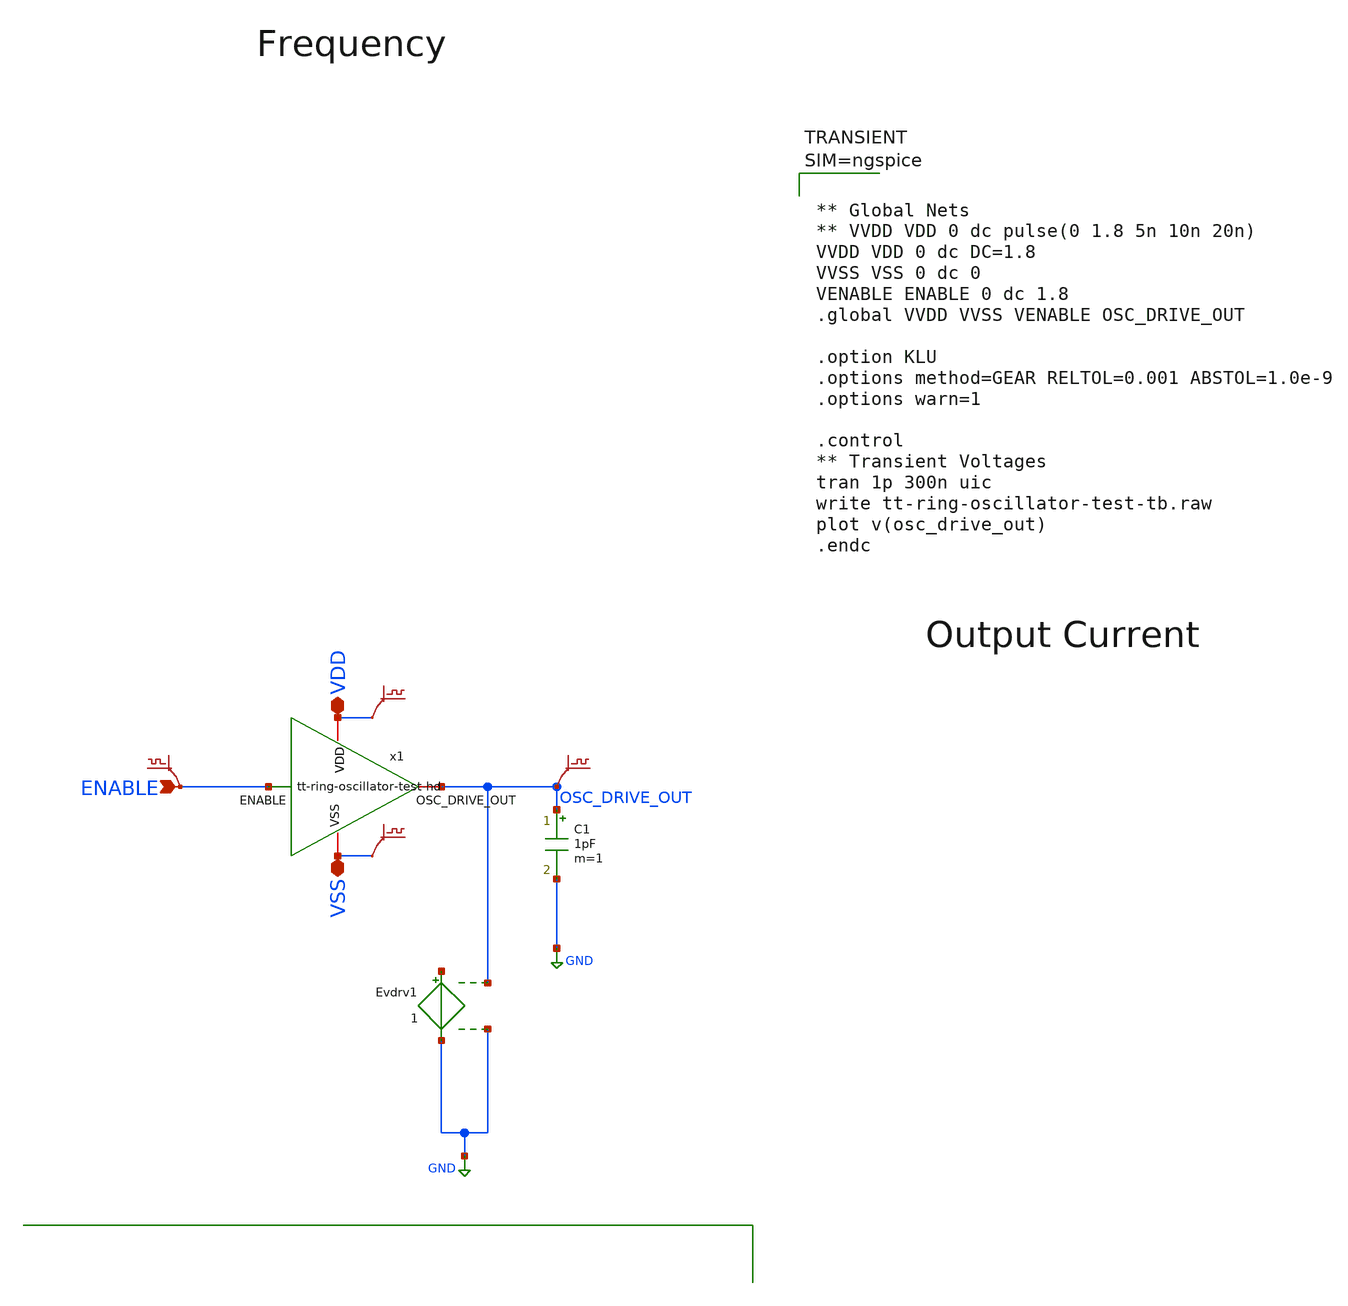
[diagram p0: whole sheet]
** sch_path: xschem/tt-ring-oscillator-test-tb.sch
**.subckt tt-ring-oscillator-test-tb ENABLE VDD VSS
*.ipin ENABLE
*.iopin VDD
*.iopin VSS
C1 OSC_DRIVE_OUT GND 1pF m=1
Evdrv1 net1 GND OSC_DRIVE_OUT GND 1
.save v(osc_drive_out)
.save v(enable)
.save i(vvdd)
.save v(vdd)
.save i(vvss)
.save v(vss)
x1 VDD VSS OSC_DRIVE_OUT ENABLE tt-ring-oscillator-test-hd
**** begin user architecture code

.lib     $::SKYWATER_MODELS/sky130.lib.spice tt
.include $::SKYWATER_STDCELLS/sky130_fd_sc_hd.spice




** Global Nets
** VVDD VDD 0 dc pulse(0 1.8 5n 10n 20n)
VVDD VDD 0 dc DC=1.8
VVSS VSS 0 dc 0
VENABLE ENABLE 0 dc 1.8
.global VVDD VVSS VENABLE OSC_DRIVE_OUT

.option KLU
.options method=GEAR RELTOL=0.001 ABSTOL=1.0e-9
.options warn=1

.control
** Transient Voltages
tran 1p 300n uic
write tt-ring-oscillator-test-tb.raw
plot v(osc_drive_out)
.endc



**** end user architecture code
**.ends

* expanding   symbol:  tt-ring-oscillator-test-hd.sym # of pins=4
** sym_path: xschem/tt-ring-oscillator-test-hd.sym
** sch_path: xschem/tt-ring-oscillator-test-hd.sch
.subckt tt-ring-oscillator-test-hd VDD VSS OSC_DRIVE_OUT ENABLE
*.ipin ENABLE
*.iopin VDD
*.iopin VSS
*.opin OSC_DRIVE_OUT
x1 net29 VSS VSS VDD VDD net1 sky130_fd_sc_hd__inv_1
x2 net1 VSS VSS VDD VDD net9 sky130_fd_sc_hd__inv_1
x3 net9 VSS VSS VDD VDD net2 sky130_fd_sc_hd__inv_1
x4 net2 VSS VSS VDD VDD net22 sky130_fd_sc_hd__inv_1
x5 net22 VSS VSS VDD VDD net21 sky130_fd_sc_hd__inv_1
x6 net21 VSS VSS VDD VDD net20 sky130_fd_sc_hd__inv_1
x7 net20 VSS VSS VDD VDD net27 sky130_fd_sc_hd__inv_1
x9 net27 VSS VSS VDD VDD net10 sky130_fd_sc_hd__inv_1
x10 net10 VSS VSS VDD VDD net3 sky130_fd_sc_hd__inv_1
x11 net3 VSS VSS VDD VDD net23 sky130_fd_sc_hd__inv_1
x12 net23 VSS VSS VDD VDD net4 sky130_fd_sc_hd__inv_1
x13 net4 VSS VSS VDD VDD net5 sky130_fd_sc_hd__inv_1
x14 net5 VSS VSS VDD VDD net30 sky130_fd_sc_hd__inv_1
x15 net30 VSS VSS VDD VDD net31 sky130_fd_sc_hd__inv_1
x16 net31 VSS VSS VDD VDD net6 sky130_fd_sc_hd__inv_1
x17 net6 VSS VSS VDD VDD net7 sky130_fd_sc_hd__inv_1
x18 net7 VSS VSS VDD VDD net8 sky130_fd_sc_hd__inv_1
x19 net8 VSS VSS VDD VDD net26 sky130_fd_sc_hd__inv_1
x20 net26 VSS VSS VDD VDD net25 sky130_fd_sc_hd__inv_1
x21 net25 VSS VSS VDD VDD net24 sky130_fd_sc_hd__inv_1
x22 net24 VSS VSS VDD VDD net28 sky130_fd_sc_hd__inv_1
x8 ENABLE net29 VSS VSS VDD VDD net13 sky130_fd_sc_hd__nand2_1
x24 net13 net11 VSS VSS VDD VDD net12 net11 sky130_fd_sc_hd__dfxbp_2
x23 net28 VSS VSS VDD VDD net14 sky130_fd_sc_hd__inv_1
x25 net14 VSS VSS VDD VDD net15 sky130_fd_sc_hd__inv_1
x26 net15 VSS VSS VDD VDD net16 sky130_fd_sc_hd__inv_1
x27 net16 VSS VSS VDD VDD net17 sky130_fd_sc_hd__inv_1
x28 net17 VSS VSS VDD VDD net18 sky130_fd_sc_hd__inv_1
x29 net18 VSS VSS VDD VDD net29 sky130_fd_sc_hd__inv_1
XM9 net19 net12 VDD VDD sky130_fd_pr__pfet_01v8 L=0.15 W=9 nf=2 ad='int((nf+1)/2) * W/nf * 0.29' as='int((nf+2)/2) * W/nf * 0.29'
+ pd='2*int((nf+1)/2) * (W/nf + 0.29)' ps='2*int((nf+2)/2) * (W/nf + 0.29)' nrd='0.29 / W' nrs='0.29 / W'
+ sa=0 sb=0 sd=0 mult=1 m=1
XM10 net19 net12 VSS VSS sky130_fd_pr__nfet_01v8 L=0.15 W=3 nf=1 ad='int((nf+1)/2) * W/nf * 0.29' as='int((nf+2)/2) * W/nf * 0.29'
+ pd='2*int((nf+1)/2) * (W/nf + 0.29)' ps='2*int((nf+2)/2) * (W/nf + 0.29)' nrd='0.29 / W' nrs='0.29 / W'
+ sa=0 sb=0 sd=0 mult=1 m=1
XM11 OSC_DRIVE_OUT net19 VDD VDD sky130_fd_pr__pfet_01v8 L=0.15 W=72 nf=8 ad='int((nf+1)/2) * W/nf * 0.29'
+ as='int((nf+2)/2) * W/nf * 0.29' pd='2*int((nf+1)/2) * (W/nf + 0.29)' ps='2*int((nf+2)/2) * (W/nf + 0.29)'
+ nrd='0.29 / W' nrs='0.29 / W' sa=0 sb=0 sd=0 mult=1 m=1
XM12 OSC_DRIVE_OUT net19 VSS VSS sky130_fd_pr__nfet_01v8 L=0.15 W=24 nf=4 ad='int((nf+1)/2) * W/nf * 0.29'
+ as='int((nf+2)/2) * W/nf * 0.29' pd='2*int((nf+1)/2) * (W/nf + 0.29)' ps='2*int((nf+2)/2) * (W/nf + 0.29)'
+ nrd='0.29 / W' nrs='0.29 / W' sa=0 sb=0 sd=0 mult=1 m=1
XC1 net20 net10 sky130_fd_pr__cap_mim_m3_1 W=2 L=2 MF=1 m=1
XC2 net21 net3 sky130_fd_pr__cap_mim_m3_1 W=2 L=2 MF=1 m=1
XC4 net10 net24 sky130_fd_pr__cap_mim_m3_1 W=2 L=2 MF=1 m=1
XC5 net3 net25 sky130_fd_pr__cap_mim_m3_1 W=2 L=2 MF=1 m=1
XC7 net24 net14 sky130_fd_pr__cap_mim_m3_1 W=2 L=2 MF=1 m=1
XC8 net25 net15 sky130_fd_pr__cap_mim_m3_1 W=2 L=2 MF=1 m=1
XC3 net22 net23 sky130_fd_pr__cap_mim_m3_1 W=2 L=2 MF=1 m=1
XC6 net23 net26 sky130_fd_pr__cap_mim_m3_1 W=2 L=2 MF=1 m=1
XC9 net26 net16 sky130_fd_pr__cap_mim_m3_1 W=2 L=2 MF=1 m=1
.ends

.GLOBAL GND
.end
